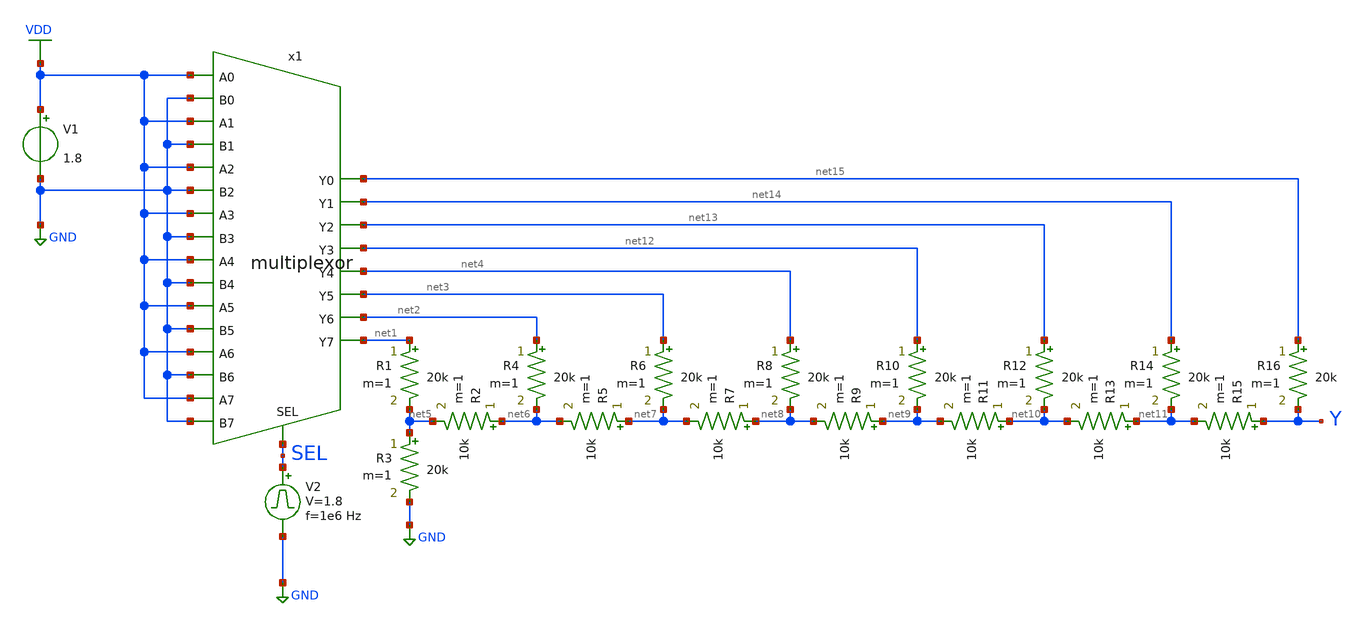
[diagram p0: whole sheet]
** sch_path: library/xschem/inv_tb.sch
**.subckt inv_tb
V1 VDD GND 1.8
V2 SEL GND pulse 0 1.8 '0.495/ 1e6 ' '0.01/1e6 ' '0.01/1e6 ' '0.49/1e6 ' '1/1e6 '
x1 VDD net15 GND VDD net14 GND VDD net13 GND VDD net12 GND VDD SEL net4 GND VDD net3 GND VDD net2
+ GND VDD net1 GND multiplexor
R1 net1 net5 20k m=1
R2 net6 net5 10k m=1
R3 net5 GND 20k m=1
R4 net2 net6 20k m=1
R5 net7 net6 10k m=1
R6 net3 net7 20k m=1
R7 net8 net7 10k m=1
R8 net4 net8 20k m=1
R9 net9 net8 10k m=1
R10 net12 net9 20k m=1
R11 net10 net9 10k m=1
R12 net13 net10 20k m=1
R13 net11 net10 10k m=1
R14 net14 net11 20k m=1
R15 Y net11 10k m=1
R16 net15 Y 20k m=1
**** begin user architecture code


.control
save all
tran 1n 2u
plot V(SEL) V(Y)+2
.endc


** opencircuitdesign pdks install
.lib $::SKYWATER_MODELS/sky130.lib.spice tt


**** end user architecture code
**.ends

* expanding   symbol:  multiplexor.sym # of pins=25
** sym_path: library/xschem/multiplexor.sym
** sch_path: library/xschem/multiplexor.sch
.subckt multiplexor A0 Y0 B0 A1 Y1 B1 A2 Y2 B2 A3 Y3 B3 A4 SEL Y4 B4 A5 Y5 B5 A6 Y6 B6 A7 Y7 B7
*.ipin A2
*.opin Y2
*.ipin B2
*.ipin A3
*.opin Y3
*.ipin B3
*.ipin A0
*.opin Y0
*.ipin B0
*.ipin A1
*.opin Y1
*.ipin B1
*.ipin A6
*.opin Y6
*.ipin B6
*.ipin A7
*.opin Y7
*.ipin B7
*.ipin A4
*.opin Y4
*.ipin B4
*.ipin A5
*.opin Y5
*.ipin B5
*.ipin SEL
x1 A2 net1 SEL nand2
x2 net17 net2 B2 nand2
x3 net1 Y2 net2 nand2
x4 A3 net3 SEL nand2
x5 net17 net4 B3 nand2
x6 net3 Y3 net4 nand2
x7 A0 net5 SEL nand2
x8 net17 net6 B0 nand2
x9 net5 Y0 net6 nand2
x10 A1 net7 SEL nand2
x11 net17 net8 B1 nand2
x12 net7 Y1 net8 nand2
x13 A6 net9 SEL nand2
x14 net17 net10 B6 nand2
x15 net9 Y6 net10 nand2
x16 A7 net11 SEL nand2
x17 net17 net12 B7 nand2
x18 net11 Y7 net12 nand2
x19 A4 net13 SEL nand2
x20 net17 net14 B4 nand2
x21 net13 Y4 net14 nand2
x22 A5 net15 SEL nand2
x23 net17 net16 B5 nand2
x24 net15 Y5 net16 nand2
x25 SEL net17 inv
.ends


* expanding   symbol:  nand2.sym # of pins=3
** sym_path: library/xschem/nand2.sym
** sch_path: library/xschem/nand2.sch
.subckt nand2 A Y B
*.opin Y
*.ipin A
*.ipin B
XM1 Y B net1 GND sky130_fd_pr__nfet_01v8 L=0.15 W=1 nf=1 ad='int((nf+1)/2) * W/nf * 0.29' as='int((nf+2)/2) * W/nf * 0.29'
+ pd='2*int((nf+1)/2) * (W/nf + 0.29)' ps='2*int((nf+2)/2) * (W/nf + 0.29)' nrd='0.29 / W' nrs='0.29 / W'
+ sa=0 sb=0 sd=0 mult=1 m=1
XM2 Y B VDD VDD sky130_fd_pr__pfet_01v8 L=0.15 W=1 nf=1 ad='int((nf+1)/2) * W/nf * 0.29' as='int((nf+2)/2) * W/nf * 0.29'
+ pd='2*int((nf+1)/2) * (W/nf + 0.29)' ps='2*int((nf+2)/2) * (W/nf + 0.29)' nrd='0.29 / W' nrs='0.29 / W'
+ sa=0 sb=0 sd=0 mult=1 m=1
XM3 Y A VDD VDD sky130_fd_pr__pfet_01v8 L=0.15 W=1 nf=1 ad='int((nf+1)/2) * W/nf * 0.29' as='int((nf+2)/2) * W/nf * 0.29'
+ pd='2*int((nf+1)/2) * (W/nf + 0.29)' ps='2*int((nf+2)/2) * (W/nf + 0.29)' nrd='0.29 / W' nrs='0.29 / W'
+ sa=0 sb=0 sd=0 mult=1 m=1
XM4 net1 A GND GND sky130_fd_pr__nfet_01v8 L=0.15 W=1 nf=1 ad='int((nf+1)/2) * W/nf * 0.29' as='int((nf+2)/2) * W/nf * 0.29'
+ pd='2*int((nf+1)/2) * (W/nf + 0.29)' ps='2*int((nf+2)/2) * (W/nf + 0.29)' nrd='0.29 / W' nrs='0.29 / W'
+ sa=0 sb=0 sd=0 mult=1 m=1
.ends


* expanding   symbol:  inv.sym # of pins=2
** sym_path: library/xschem/inv.sym
** sch_path: library/xschem/inv.sch
.subckt inv A Y
*.opin Y
*.ipin A
XM1 Y A GND GND sky130_fd_pr__nfet_01v8 L=0.15 W=1 nf=1 ad='int((nf+1)/2) * W/nf * 0.29' as='int((nf+2)/2) * W/nf * 0.29'
+ pd='2*int((nf+1)/2) * (W/nf + 0.29)' ps='2*int((nf+2)/2) * (W/nf + 0.29)' nrd='0.29 / W' nrs='0.29 / W'
+ sa=0 sb=0 sd=0 mult=1 m=1
XM2 Y A VDD VDD sky130_fd_pr__pfet_01v8 L=0.15 W=1 nf=1 ad='int((nf+1)/2) * W/nf * 0.29' as='int((nf+2)/2) * W/nf * 0.29'
+ pd='2*int((nf+1)/2) * (W/nf + 0.29)' ps='2*int((nf+2)/2) * (W/nf + 0.29)' nrd='0.29 / W' nrs='0.29 / W'
+ sa=0 sb=0 sd=0 mult=1 m=1
.ends

.GLOBAL VDD
.GLOBAL GND
.end
